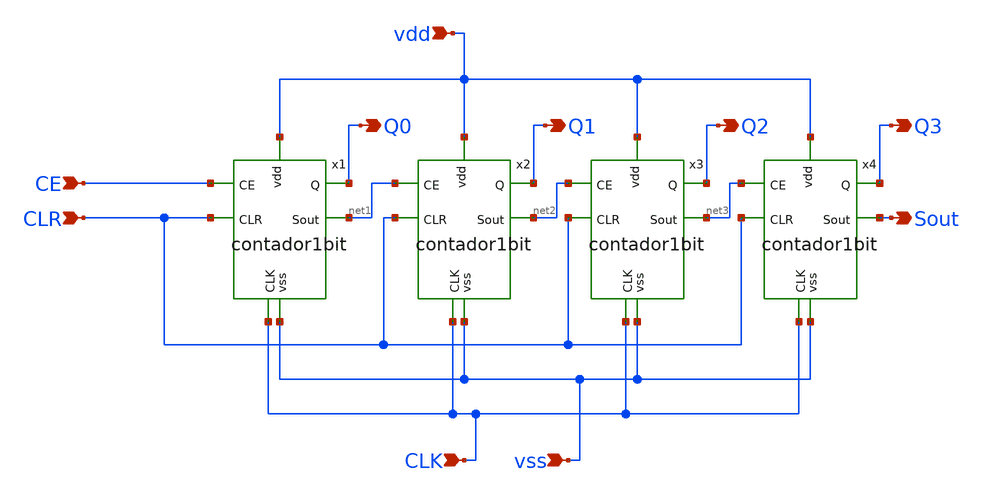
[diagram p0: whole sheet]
** sch_path: track_vlsi/lapi-fernandez/sch/contador4bits.sch
**.subckt contador4bits CE CLR vdd CLK vss Q0 Q1 Q2 Q3 Sout
*.ipin CE
*.ipin CLR
*.ipin vdd
*.ipin CLK
*.ipin vss
*.opin Q0
*.opin Q1
*.opin Q2
*.opin Q3
*.opin Sout
x1 vdd Q0 net1 CLK CLR CE vss contador1bit
x2 vdd Q1 net2 CLK CLR net1 vss contador1bit
x3 vdd Q2 net3 CLK CLR net2 vss contador1bit
x4 vdd Q3 Sout CLK CLR net3 vss contador1bit
**.ends
.end
